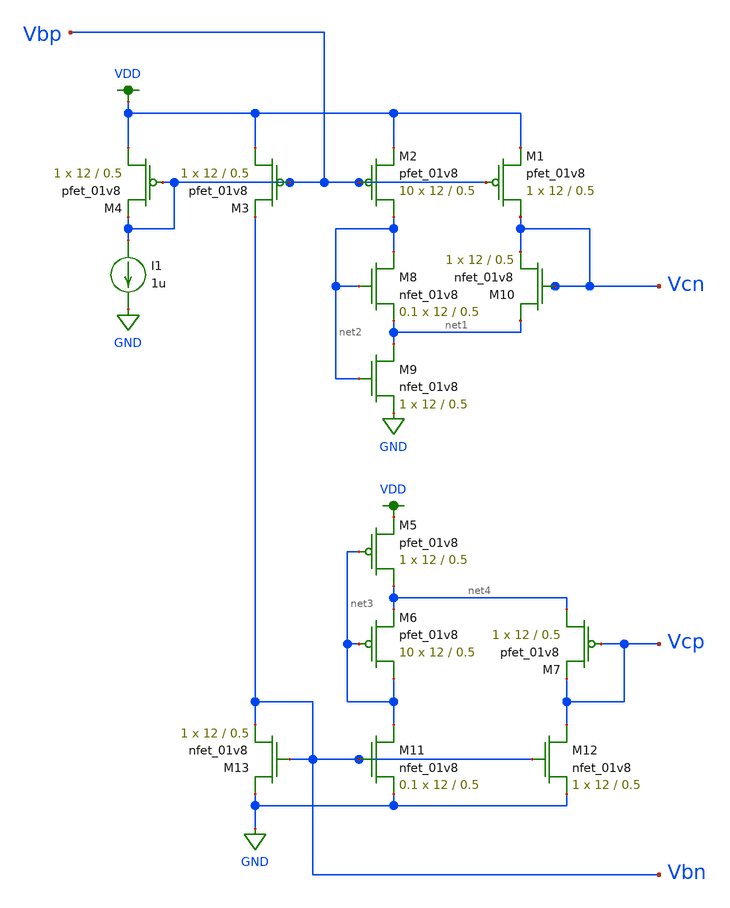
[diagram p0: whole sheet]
** sch_path: MP3/bias.sch
**.subckt bias
XM1 Vcn Vbp VDD VDD sky130_fd_pr__pfet_01v8 L=0.5 W=12 nf=1 ad='int((nf+1)/2) * W/nf * 0.29' as='int((nf+2)/2) * W/nf * 0.29'
+ pd='2*int((nf+1)/2) * (W/nf + 0.29)' ps='2*int((nf+2)/2) * (W/nf + 0.29)' nrd='0.29 / W' nrs='0.29 / W'
+ sa=0 sb=0 sd=0 mult=1 m=1
XM2 net2 Vbp VDD VDD sky130_fd_pr__pfet_01v8 L=0.5 W=12 nf=1 ad='int((nf+1)/2) * W/nf * 0.29' as='int((nf+2)/2) * W/nf * 0.29'
+ pd='2*int((nf+1)/2) * (W/nf + 0.29)' ps='2*int((nf+2)/2) * (W/nf + 0.29)' nrd='0.29 / W' nrs='0.29 / W'
+ sa=0 sb=0 sd=0 mult=10 m=10
XM3 VDD Vbp Vbn VDD sky130_fd_pr__pfet_01v8 L=0.5 W=12 nf=1 ad='int((nf+1)/2) * W/nf * 0.29' as='int((nf+2)/2) * W/nf * 0.29'
+ pd='2*int((nf+1)/2) * (W/nf + 0.29)' ps='2*int((nf+2)/2) * (W/nf + 0.29)' nrd='0.29 / W' nrs='0.29 / W'
+ sa=0 sb=0 sd=0 mult=1 m=1
XM4 VDD Vbp Vbp VDD sky130_fd_pr__pfet_01v8 L=0.5 W=12 nf=1 ad='int((nf+1)/2) * W/nf * 0.29' as='int((nf+2)/2) * W/nf * 0.29'
+ pd='2*int((nf+1)/2) * (W/nf + 0.29)' ps='2*int((nf+2)/2) * (W/nf + 0.29)' nrd='0.29 / W' nrs='0.29 / W'
+ sa=0 sb=0 sd=0 mult=1 m=1
XM5 net4 net3 VDD VDD sky130_fd_pr__pfet_01v8 L=0.5 W=12 nf=1 ad='int((nf+1)/2) * W/nf * 0.29' as='int((nf+2)/2) * W/nf * 0.29'
+ pd='2*int((nf+1)/2) * (W/nf + 0.29)' ps='2*int((nf+2)/2) * (W/nf + 0.29)' nrd='0.29 / W' nrs='0.29 / W'
+ sa=0 sb=0 sd=0 mult=1 m=1
XM6 net3 net3 net4 VDD sky130_fd_pr__pfet_01v8 L=0.5 W=12 nf=1 ad='int((nf+1)/2) * W/nf * 0.29' as='int((nf+2)/2) * W/nf * 0.29'
+ pd='2*int((nf+1)/2) * (W/nf + 0.29)' ps='2*int((nf+2)/2) * (W/nf + 0.29)' nrd='0.29 / W' nrs='0.29 / W'
+ sa=0 sb=0 sd=0 mult=10 m=10
XM7 net4 Vcp Vcp VDD sky130_fd_pr__pfet_01v8 L=0.5 W=12 nf=1 ad='int((nf+1)/2) * W/nf * 0.29' as='int((nf+2)/2) * W/nf * 0.29'
+ pd='2*int((nf+1)/2) * (W/nf + 0.29)' ps='2*int((nf+2)/2) * (W/nf + 0.29)' nrd='0.29 / W' nrs='0.29 / W'
+ sa=0 sb=0 sd=0 mult=1 m=1
XM8 net2 net2 net1 GND sky130_fd_pr__nfet_01v8 L=0.5 W=12 nf=1 ad='int((nf+1)/2) * W/nf * 0.29' as='int((nf+2)/2) * W/nf * 0.29'
+ pd='2*int((nf+1)/2) * (W/nf + 0.29)' ps='2*int((nf+2)/2) * (W/nf + 0.29)' nrd='0.29 / W' nrs='0.29 / W'
+ sa=0 sb=0 sd=0 mult=0.1 m=0.1
XM9 net1 net2 GND GND sky130_fd_pr__nfet_01v8 L=0.5 W=12 nf=1 ad='int((nf+1)/2) * W/nf * 0.29' as='int((nf+2)/2) * W/nf * 0.29'
+ pd='2*int((nf+1)/2) * (W/nf + 0.29)' ps='2*int((nf+2)/2) * (W/nf + 0.29)' nrd='0.29 / W' nrs='0.29 / W'
+ sa=0 sb=0 sd=0 mult=1 m=1
XM10 net1 Vcn Vcn GND sky130_fd_pr__nfet_01v8 L=0.5 W=12 nf=1 ad='int((nf+1)/2) * W/nf * 0.29' as='int((nf+2)/2) * W/nf * 0.29'
+ pd='2*int((nf+1)/2) * (W/nf + 0.29)' ps='2*int((nf+2)/2) * (W/nf + 0.29)' nrd='0.29 / W' nrs='0.29 / W'
+ sa=0 sb=0 sd=0 mult=1 m=1
XM11 net3 Vbn GND GND sky130_fd_pr__nfet_01v8 L=0.5 W=12 nf=1 ad='int((nf+1)/2) * W/nf * 0.29' as='int((nf+2)/2) * W/nf * 0.29'
+ pd='2*int((nf+1)/2) * (W/nf + 0.29)' ps='2*int((nf+2)/2) * (W/nf + 0.29)' nrd='0.29 / W' nrs='0.29 / W'
+ sa=0 sb=0 sd=0 mult=0.1 m=0.1
XM12 Vcp Vbn GND GND sky130_fd_pr__nfet_01v8 L=0.5 W=12 nf=1 ad='int((nf+1)/2) * W/nf * 0.29' as='int((nf+2)/2) * W/nf * 0.29'
+ pd='2*int((nf+1)/2) * (W/nf + 0.29)' ps='2*int((nf+2)/2) * (W/nf + 0.29)' nrd='0.29 / W' nrs='0.29 / W'
+ sa=0 sb=0 sd=0 mult=1 m=1
XM13 GND Vbn Vbn GND sky130_fd_pr__nfet_01v8 L=0.5 W=12 nf=1 ad='int((nf+1)/2) * W/nf * 0.29' as='int((nf+2)/2) * W/nf * 0.29'
+ pd='2*int((nf+1)/2) * (W/nf + 0.29)' ps='2*int((nf+2)/2) * (W/nf + 0.29)' nrd='0.29 / W' nrs='0.29 / W'
+ sa=0 sb=0 sd=0 mult=1 m=1
I1 Vbp GND 1u
**.ends
.GLOBAL VDD
.GLOBAL GND
.end
